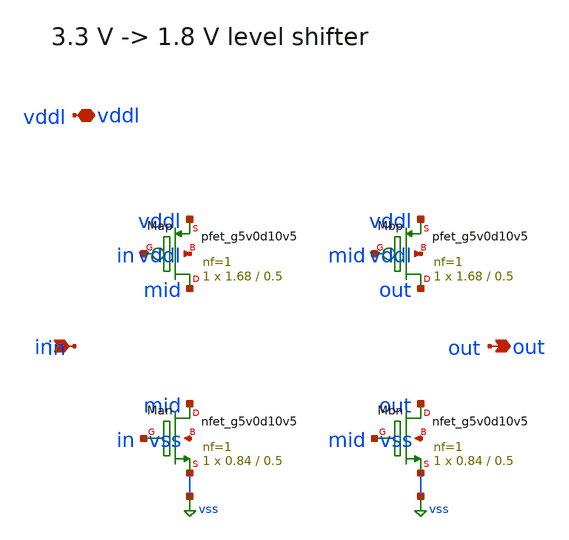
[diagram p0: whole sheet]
** sch_path: xschem/rt5w_lsdn.sch
**.subckt rt5w_lsdn in out vddl
*.ipin in
*.opin out
*.iopin vddl
XMap mid in vddl vddl sky130_fd_pr__pfet_g5v0d10v5 L=0.5 W=1.68 nf=1 ad=0.4872 as=0.4872 pd=3.94
+ ps=3.94 nrd=0.1726 nrs=0.1726 sa=0 sb=0 sd=0 mult=1 m=1
XMan mid in vss vss sky130_fd_pr__nfet_g5v0d10v5 L=0.5 W=0.84 nf=1 ad=0.2436 as=0.2436 pd=2.26
+ ps=2.26 nrd=0.3452 nrs=0.3452 sa=0 sb=0 sd=0 mult=1 m=1
XMbp out mid vddl vddl sky130_fd_pr__pfet_g5v0d10v5 L=0.5 W=1.68 nf=1 ad=0.4872 as=0.4872 pd=3.94
+ ps=3.94 nrd=0.1726 nrs=0.1726 sa=0 sb=0 sd=0 mult=1 m=1
XMbn out mid vss vss sky130_fd_pr__nfet_g5v0d10v5 L=0.5 W=0.84 nf=1 ad=0.2436 as=0.2436 pd=2.26
+ ps=2.26 nrd=0.3452 nrs=0.3452 sa=0 sb=0 sd=0 mult=1 m=1
**.ends
.GLOBAL vss
.end
